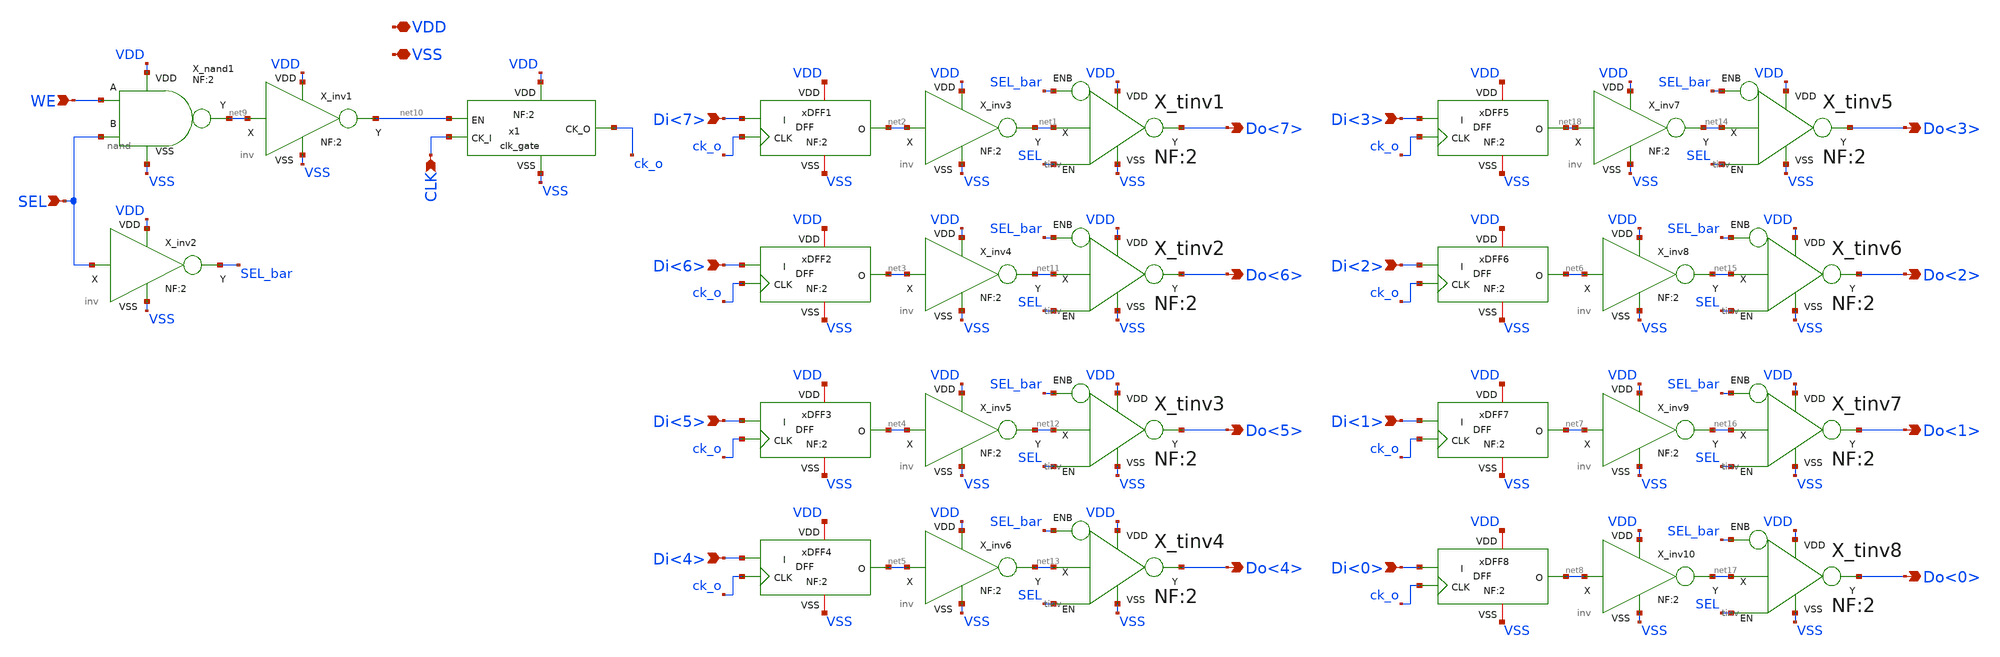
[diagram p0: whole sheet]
** sch_path: xschem_lib/DFFRAM_full_custom/byte_dff.sch
**.subckt byte_dff Do<7> Di<7> Do<6> Di<6> Do<5> Di<5> Do<4> Di<4> Do<3> Di<3> Do<2> Di<2> Do<1>
*+ Di<1> Do<0> Di<0> WE SEL CLK VDD VSS
*.opin Do<7>
*.ipin Di<7>
*.opin Do<6>
*.ipin Di<6>
*.opin Do<5>
*.ipin Di<5>
*.opin Do<4>
*.ipin Di<4>
*.opin Do<3>
*.ipin Di<3>
*.opin Do<2>
*.ipin Di<2>
*.opin Do<1>
*.ipin Di<1>
*.opin Do<0>
*.ipin Di<0>
*.ipin WE
*.ipin SEL
*.ipin CLK
*.iopin VDD
*.iopin VSS
X_nand1 SEL WE net9 VDD VSS nand NF=2
X_inv1 net9 VDD VSS net10 inv NF=2
X_inv2 SEL VDD VSS SEL_bar inv NF=2
x1 VDD net10 ck_o CLK VSS clk_gate NF=2
xDFF1 VDD VSS Di<7> net2 ck_o DFF NF=2
X_tinv1 net1 SEL SEL_bar VDD VSS Do<7> tinv NF=2
X_inv3 net2 VDD VSS net1 inv NF=2
xDFF2 VDD VSS Di<6> net3 ck_o DFF NF=2
xDFF3 VDD VSS Di<5> net4 ck_o DFF NF=2
xDFF4 VDD VSS Di<4> net5 ck_o DFF NF=2
xDFF5 VDD VSS Di<3> net18 ck_o DFF NF=2
xDFF6 VDD VSS Di<2> net6 ck_o DFF NF=2
xDFF7 VDD VSS Di<1> net7 ck_o DFF NF=2
xDFF8 VDD VSS Di<0> net8 ck_o DFF NF=2
X_tinv2 net11 SEL SEL_bar VDD VSS Do<6> tinv NF=2
X_inv4 net3 VDD VSS net11 inv NF=2
X_tinv3 net12 SEL SEL_bar VDD VSS Do<5> tinv NF=2
X_inv5 net4 VDD VSS net12 inv NF=2
X_tinv4 net13 SEL SEL_bar VDD VSS Do<4> tinv NF=2
X_inv6 net5 VDD VSS net13 inv NF=2
X_tinv5 net14 SEL SEL_bar VDD VSS Do<3> tinv NF=2
X_inv7 net18 VDD VSS net14 inv NF=2
X_tinv6 net15 SEL SEL_bar VDD VSS Do<2> tinv NF=2
X_inv8 net6 VDD VSS net15 inv NF=2
X_tinv7 net16 SEL SEL_bar VDD VSS Do<1> tinv NF=2
X_inv9 net7 VDD VSS net16 inv NF=2
X_tinv8 net17 SEL SEL_bar VDD VSS Do<0> tinv NF=2
X_inv10 net8 VDD VSS net17 inv NF=2
**.ends
.end
